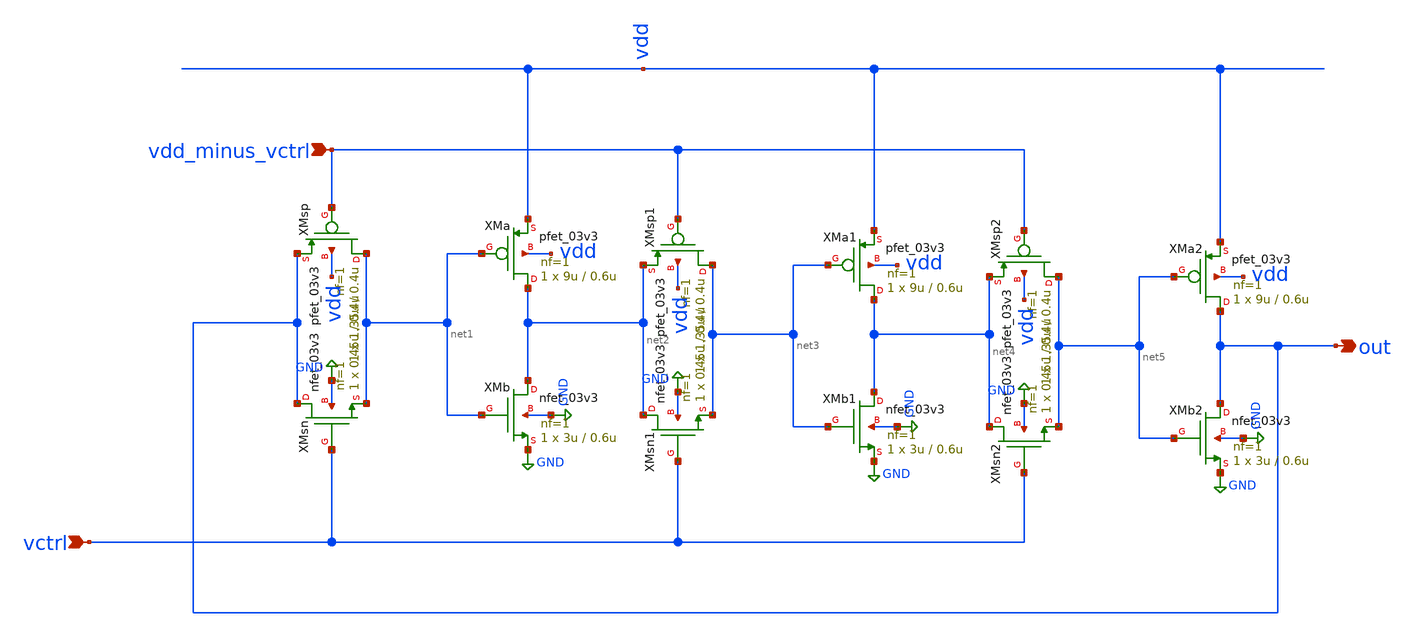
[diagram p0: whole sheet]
** sch_path: verified/0001_vco.sch
**.subckt 0001_vco out vctrl vdd_minus_vctrl
*.opin out
*.ipin vctrl
*.ipin vdd_minus_vctrl
XMsn out vctrl net1 GND nfet_03v3 L=0.4u W=0.45u nf=1 ad='int((nf+1)/2) * W/nf * 0.18u' as='int((nf+2)/2) * W/nf * 0.18u'
+ pd='2*int((nf+1)/2) * (W/nf + 0.18u)' ps='2*int((nf+2)/2) * (W/nf + 0.18u)' nrd='0.18u / W' nrs='0.18u / W'
+ sa=0 sb=0 sd=0 m=1
XMsp net1 vdd_minus_vctrl out vdd pfet_03v3 L=0.4u W=1.35u nf=1 ad='int((nf+1)/2) * W/nf * 0.18u' as='int((nf+2)/2) * W/nf * 0.18u'
+ pd='2*int((nf+1)/2) * (W/nf + 0.18u)' ps='2*int((nf+2)/2) * (W/nf + 0.18u)' nrd='0.18u / W' nrs='0.18u / W'
+ sa=0 sb=0 sd=0 m=1
XMa net2 net1 vdd vdd pfet_03v3 L=0.6u W=9u nf=1 ad='int((nf+1)/2) * W/nf * 0.18u' as='int((nf+2)/2) * W/nf * 0.18u'
+ pd='2*int((nf+1)/2) * (W/nf + 0.18u)' ps='2*int((nf+2)/2) * (W/nf + 0.18u)' nrd='0.18u / W' nrs='0.18u / W'
+ sa=0 sb=0 sd=0 m=1
XMb net2 net1 GND GND nfet_03v3 L=0.6u W=3u nf=1 ad='int((nf+1)/2) * W/nf * 0.18u' as='int((nf+2)/2) * W/nf * 0.18u'
+ pd='2*int((nf+1)/2) * (W/nf + 0.18u)' ps='2*int((nf+2)/2) * (W/nf + 0.18u)' nrd='0.18u / W' nrs='0.18u / W'
+ sa=0 sb=0 sd=0 m=1
XMsn1 net2 vctrl net3 GND nfet_03v3 L=0.4u W=0.45u nf=1 ad='int((nf+1)/2) * W/nf * 0.18u' as='int((nf+2)/2) * W/nf * 0.18u'
+ pd='2*int((nf+1)/2) * (W/nf + 0.18u)' ps='2*int((nf+2)/2) * (W/nf + 0.18u)' nrd='0.18u / W' nrs='0.18u / W'
+ sa=0 sb=0 sd=0 m=1
XMsp1 net3 vdd_minus_vctrl net2 vdd pfet_03v3 L=0.4u W=1.35u nf=1 ad='int((nf+1)/2) * W/nf * 0.18u' as='int((nf+2)/2) * W/nf * 0.18u'
+ pd='2*int((nf+1)/2) * (W/nf + 0.18u)' ps='2*int((nf+2)/2) * (W/nf + 0.18u)' nrd='0.18u / W' nrs='0.18u / W'
+ sa=0 sb=0 sd=0 m=1
XMa1 net4 net3 vdd vdd pfet_03v3 L=0.6u W=9u nf=1 ad='int((nf+1)/2) * W/nf * 0.18u' as='int((nf+2)/2) * W/nf * 0.18u'
+ pd='2*int((nf+1)/2) * (W/nf + 0.18u)' ps='2*int((nf+2)/2) * (W/nf + 0.18u)' nrd='0.18u / W' nrs='0.18u / W'
+ sa=0 sb=0 sd=0 m=1
XMb1 net4 net3 GND GND nfet_03v3 L=0.6u W=3u nf=1 ad='int((nf+1)/2) * W/nf * 0.18u' as='int((nf+2)/2) * W/nf * 0.18u'
+ pd='2*int((nf+1)/2) * (W/nf + 0.18u)' ps='2*int((nf+2)/2) * (W/nf + 0.18u)' nrd='0.18u / W' nrs='0.18u / W'
+ sa=0 sb=0 sd=0 m=1
XMsn2 net4 vctrl net5 GND nfet_03v3 L=0.4u W=0.45u nf=1 ad='int((nf+1)/2) * W/nf * 0.18u' as='int((nf+2)/2) * W/nf * 0.18u'
+ pd='2*int((nf+1)/2) * (W/nf + 0.18u)' ps='2*int((nf+2)/2) * (W/nf + 0.18u)' nrd='0.18u / W' nrs='0.18u / W'
+ sa=0 sb=0 sd=0 m=1
XMsp2 net5 vdd_minus_vctrl net4 vdd pfet_03v3 L=0.4u W=1.35u nf=1 ad='int((nf+1)/2) * W/nf * 0.18u' as='int((nf+2)/2) * W/nf * 0.18u'
+ pd='2*int((nf+1)/2) * (W/nf + 0.18u)' ps='2*int((nf+2)/2) * (W/nf + 0.18u)' nrd='0.18u / W' nrs='0.18u / W'
+ sa=0 sb=0 sd=0 m=1
XMa2 out net5 vdd vdd pfet_03v3 L=0.6u W=9u nf=1 ad='int((nf+1)/2) * W/nf * 0.18u' as='int((nf+2)/2) * W/nf * 0.18u'
+ pd='2*int((nf+1)/2) * (W/nf + 0.18u)' ps='2*int((nf+2)/2) * (W/nf + 0.18u)' nrd='0.18u / W' nrs='0.18u / W'
+ sa=0 sb=0 sd=0 m=1
XMb2 out net5 GND GND nfet_03v3 L=0.6u W=3u nf=1 ad='int((nf+1)/2) * W/nf * 0.18u' as='int((nf+2)/2) * W/nf * 0.18u'
+ pd='2*int((nf+1)/2) * (W/nf + 0.18u)' ps='2*int((nf+2)/2) * (W/nf + 0.18u)' nrd='0.18u / W' nrs='0.18u / W'
+ sa=0 sb=0 sd=0 m=1
**** begin user architecture code



.include '/home/user/.volare/volare/sky130/versions/0fe599b2afb6708d281543108caf8310912f54af/volare/gf180mcu/versions/0fe599b2afb6708d281543108caf8310912f54af/gf180mcuD/libs.tech/ngspice/design.ngspice'
.lib '/home/user/.volare/volare/sky130/versions/0fe599b2afb6708d281543108caf8310912f54af/volare/gf180mcu/versions/0fe599b2afb6708d281543108caf8310912f54af/gf180mcuD/libs.tech/ngspice/sm141064.ngspice' typical

VDD vdd GND 3.3
Vctrl vctrl GND 1.5
Vvp vdd_minus_vctrl GND {3.3-1.5}

.ic v(out)=3.3 v(net2)=0 v(net4)=3.3
.tran 0.1n 500n uic
.save all
.control
run
plot v(out)
.endc


**** end user architecture code
**.ends
.GLOBAL GND
.end
